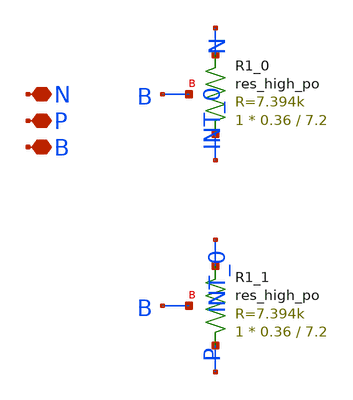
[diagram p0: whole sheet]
** sch_path: design/LELO_TEMP_SKY130A/REYATR_RES2.sch
**.subckt REYATR_RES2 N P B
*.iopin N
*.iopin P
*.iopin B
XR1_0 INT_0 N B sky130_fd_pr__res_high_po W=0.36 L=7.2 mult=1 m=1
XR1_1 P INT_0 B sky130_fd_pr__res_high_po W=0.36 L=7.2 mult=1 m=1
**.ends
.end
